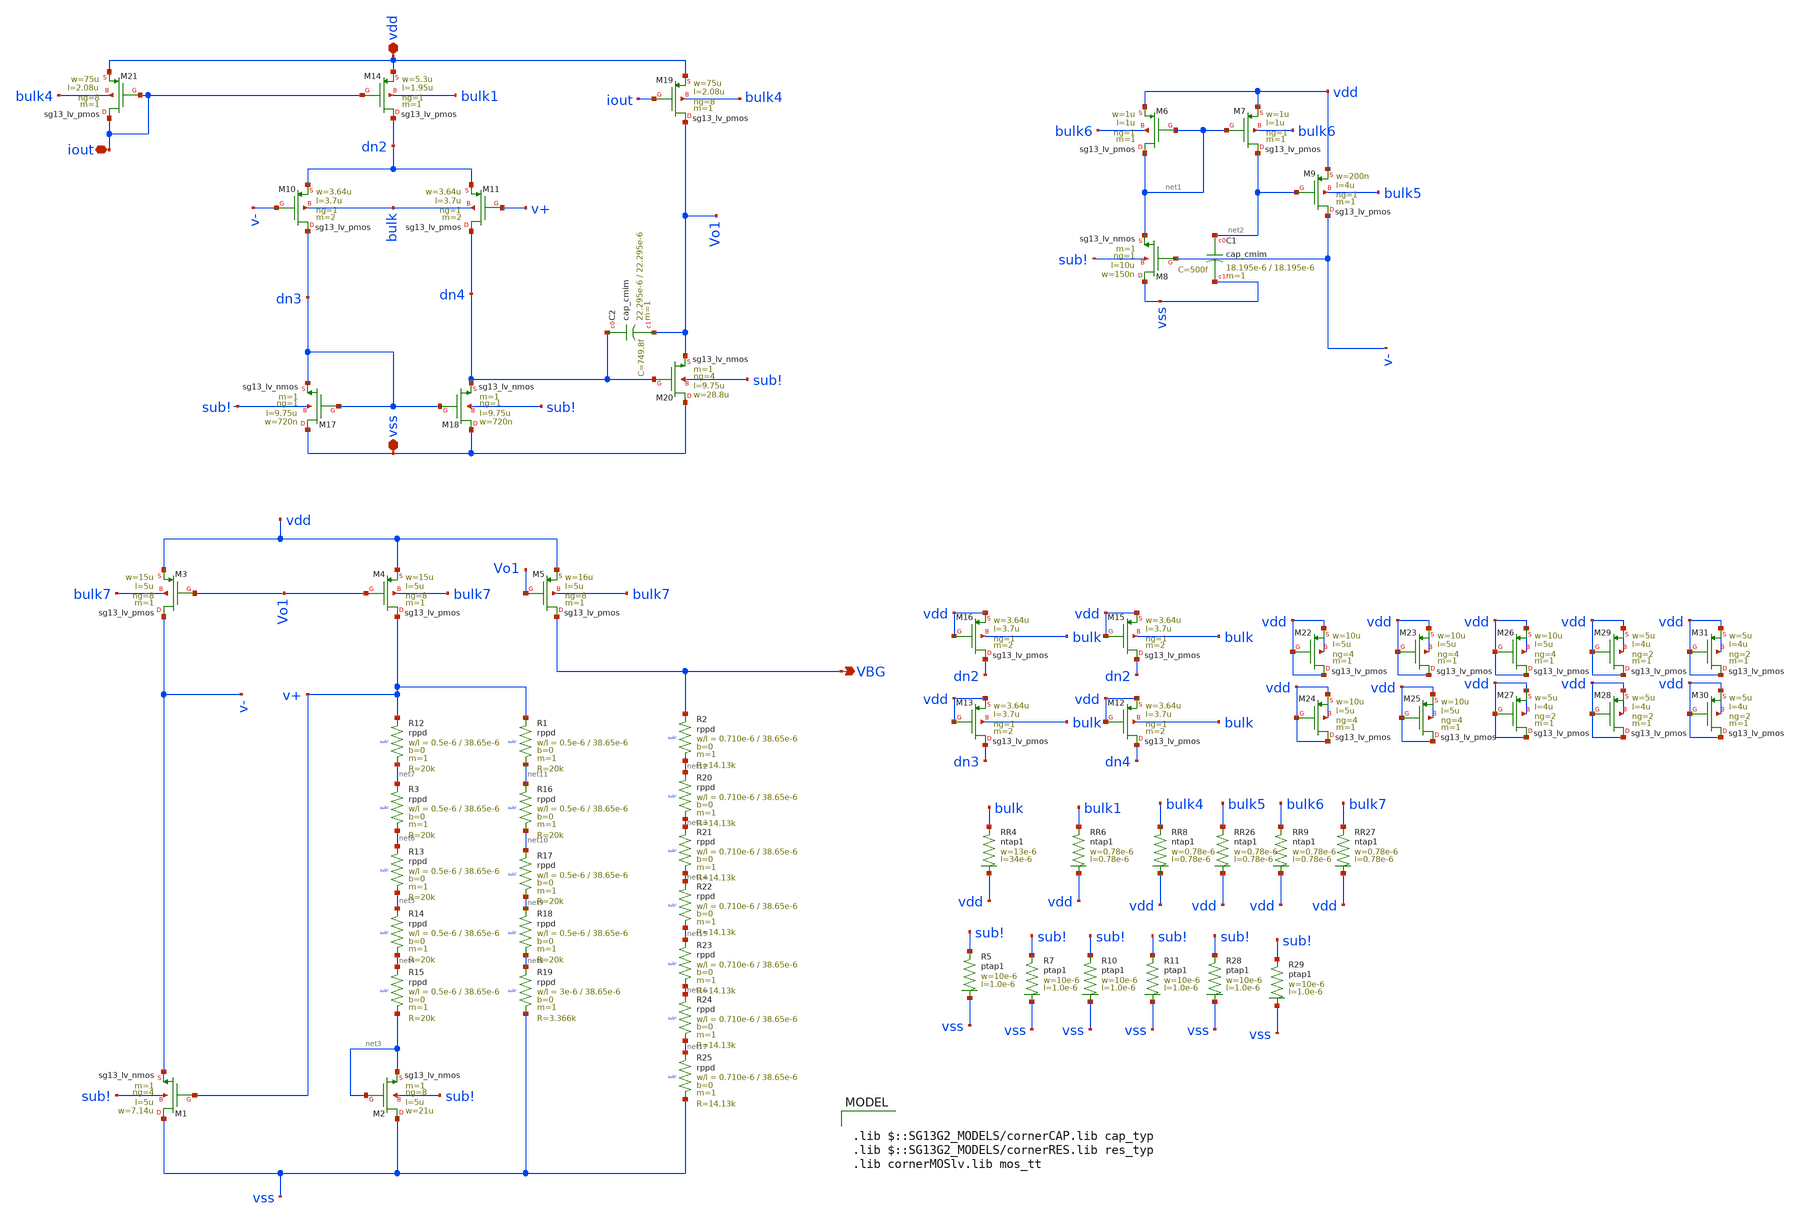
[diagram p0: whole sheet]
** sch_path: modules/module_1_bandgap_reference/part_3_layout/BGR_layout/final_bandgapreference/schematic_mod/full_bandgap.sch
**.subckt full_bandgap VBG vss vdd iout
*.opin VBG
*.iopin vss
*.iopin vdd
*.iopin iout
XM8 vss v- net1 sub! sg13_lv_nmos w=150n l=10u ng=1 m=1 mm_ok=1
XM6 net1 net1 vdd bulk6 sg13_lv_pmos w=1u l=1u ng=1 m=1 mm_ok=1
XM7 net2 net1 vdd bulk6 sg13_lv_pmos w=1u l=1u ng=1 m=1 mm_ok=1
XM9 v- net2 vdd bulk5 sg13_lv_pmos w=200n l=4u ng=1 m=1 mm_ok=1
XM1 vss v+ v- sub! sg13_lv_nmos w=7.14u l=5u ng=4 m=1 mm_ok=1
XM2 vss net3 net3 sub! sg13_lv_nmos w=21u l=5u ng=8 m=1 mm_ok=1
XM3 v- Vo1 vdd bulk7 sg13_lv_pmos w=15u l=5u ng=8 m=1 mm_ok=1
XM4 v+ Vo1 vdd bulk7 sg13_lv_pmos w=15u l=5u ng=8 m=1 mm_ok=1
XM5 VBG Vo1 vdd bulk7 sg13_lv_pmos w=16u l=5u ng=8 m=1 mm_ok=1
XR2 VBG net12 sub! rppd w=0.710e-6 l=38.65e-6 m=1 b=0 mm_ok=1
XC1 net2 vss cap_cmim w=18.195e-6 l=18.195e-6 m=1 mm_ok=1
XM10 dn3 v- dn2 bulk sg13_lv_pmos w=3.64u l=3.7u ng=1 m=2 mm_ok=1
XM11 dn4 v+ dn2 bulk sg13_lv_pmos w=3.64u l=3.7u ng=1 m=2 mm_ok=1
XM12 dn4 vdd vdd bulk sg13_lv_pmos w=3.64u l=3.7u ng=1 m=2 mm_ok=1
XM13 dn3 vdd vdd bulk sg13_lv_pmos w=3.64u l=3.7u ng=1 m=2 mm_ok=1
XM15 dn2 vdd vdd bulk sg13_lv_pmos w=3.64u l=3.7u ng=1 m=2 mm_ok=1
XM16 dn2 vdd vdd bulk sg13_lv_pmos w=3.64u l=3.7u ng=1 m=2 mm_ok=1
XR4 bulk vdd ntap1 R=1.828 w=13e-6 l=34e-6
XM14 dn2 iout vdd bulk1 sg13_lv_pmos w=5.3u l=1.95u ng=1 m=1 mm_ok=1
XR5 sub! vss ptap1 R=30.62 w=10e-6 l=1.0e-6
XR6 bulk1 vdd ntap1 R=262.8 w=0.78e-6 l=0.78e-6
XM17 vss dn3 dn3 sub! sg13_lv_nmos w=720n l=9.75u ng=1 m=1 mm_ok=1
XM18 vss dn3 dn4 sub! sg13_lv_nmos w=720n l=9.75u ng=1 m=1 mm_ok=1
XM19 Vo1 iout vdd bulk4 sg13_lv_pmos w=75u l=2.08u ng=8 m=1 mm_ok=1
XM20 vss dn4 Vo1 sub! sg13_lv_nmos w=28.8u l=9.75u ng=4 m=1 mm_ok=1
XM21 iout iout vdd bulk4 sg13_lv_pmos w=75u l=2.08u ng=8 m=1 mm_ok=1
XC2 dn4 Vo1 cap_cmim w=22.295e-6 l=22.295e-6 m=1 mm_ok=1
XR8 bulk4 vdd ntap1 R=262.8 w=0.78e-6 l=0.78e-6
XR9 bulk6 vdd ntap1 R=262.8 w=0.78e-6 l=0.78e-6
XR12 v+ net7 sub! rppd w=0.5e-6 l=38.65e-6 m=1 b=0 mm_ok=1
XR3 net7 net6 sub! rppd w=0.5e-6 l=38.65e-6 m=1 b=0 mm_ok=1
XR13 net6 net5 sub! rppd w=0.5e-6 l=38.65e-6 m=1 b=0 mm_ok=1
XR14 net5 net4 sub! rppd w=0.5e-6 l=38.65e-6 m=1 b=0 mm_ok=1
XR15 net4 net3 sub! rppd w=0.5e-6 l=38.65e-6 m=1 b=0 mm_ok=1
XR1 v+ net11 sub! rppd w=0.5e-6 l=38.65e-6 m=1 b=0 mm_ok=1
XR16 net11 net10 sub! rppd w=0.5e-6 l=38.65e-6 m=1 b=0 mm_ok=1
XR17 net10 net9 sub! rppd w=0.5e-6 l=38.65e-6 m=1 b=0 mm_ok=1
XR18 net9 net8 sub! rppd w=0.5e-6 l=38.65e-6 m=1 b=0 mm_ok=1
XR19 net8 vss sub! rppd w=3e-6 l=38.65e-6 m=1 b=0 mm_ok=1
XR20 net12 net13 sub! rppd w=0.710e-6 l=38.65e-6 m=1 b=0 mm_ok=1
XR21 net13 net14 sub! rppd w=0.710e-6 l=38.65e-6 m=1 b=0 mm_ok=1
XR22 net14 net15 sub! rppd w=0.710e-6 l=38.65e-6 m=1 b=0 mm_ok=1
XR23 net15 net16 sub! rppd w=0.710e-6 l=38.65e-6 m=1 b=0 mm_ok=1
XR24 net16 net17 sub! rppd w=0.710e-6 l=38.65e-6 m=1 b=0 mm_ok=1
XR25 net17 vss sub! rppd w=0.710e-6 l=38.65e-6 m=1 b=0 mm_ok=1
XR26 bulk5 vdd ntap1 R=262.8 w=0.78e-6 l=0.78e-6
XR27 bulk7 vdd ntap1 R=262.8 w=0.78e-6 l=0.78e-6
XM22 vdd vdd vdd vdd sg13_lv_pmos w=10u l=5u ng=4 m=1 mm_ok=1
XM23 vdd vdd vdd vdd sg13_lv_pmos w=10u l=5u ng=4 m=1 mm_ok=1
XM24 vdd vdd vdd vdd sg13_lv_pmos w=10u l=5u ng=4 m=1 mm_ok=1
XM25 vdd vdd vdd vdd sg13_lv_pmos w=10u l=5u ng=4 m=1 mm_ok=1
XM26 vdd vdd vdd vdd sg13_lv_pmos w=10u l=5u ng=4 m=1 mm_ok=1
XM27 vdd vdd vdd vdd sg13_lv_pmos w=5u l=4u ng=2 m=1 mm_ok=1
XM28 vdd vdd vdd vdd sg13_lv_pmos w=5u l=4u ng=2 m=1 mm_ok=1
XM29 vdd vdd vdd vdd sg13_lv_pmos w=5u l=4u ng=2 m=1 mm_ok=1
XM30 vdd vdd vdd vdd sg13_lv_pmos w=5u l=4u ng=2 m=1 mm_ok=1
XM31 vdd vdd vdd vdd sg13_lv_pmos w=5u l=4u ng=2 m=1 mm_ok=1
XR7 sub! vss ptap1 R=30.62 w=10e-6 l=1.0e-6
XR10 sub! vss ptap1 R=30.62 w=10e-6 l=1.0e-6
XR11 sub! vss ptap1 R=30.62 w=10e-6 l=1.0e-6
XR28 sub! vss ptap1 R=30.62 w=10e-6 l=1.0e-6
XR29 sub! vss ptap1 R=30.62 w=10e-6 l=1.0e-6
**** begin user architecture code

.lib $::SG13G2_MODELS/cornerCAP.lib cap_typ
.lib $::SG13G2_MODELS/cornerRES.lib res_typ
.lib cornerMOSlv.lib mos_tt

**** end user architecture code
**.ends
.end
